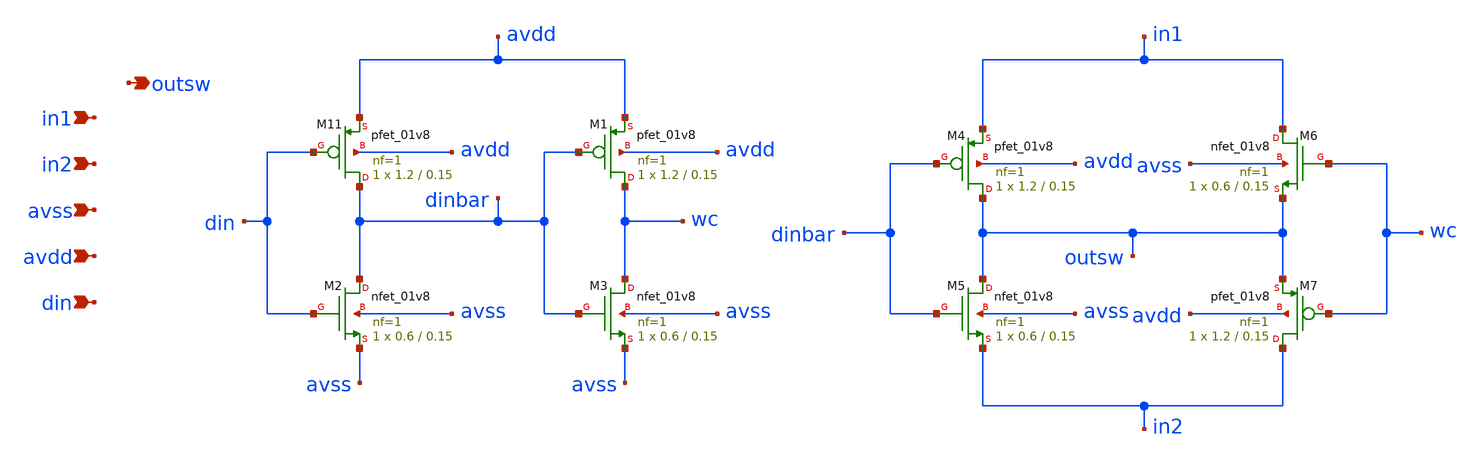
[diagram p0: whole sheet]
** sch_path: xschem/switch.sch
**.subckt switch avss avdd din in1 in2 outsw
*.ipin avss
*.ipin avdd
*.ipin din
*.ipin in1
*.ipin in2
*.opin outsw
XM11 dinbar din avdd avdd sky130_fd_pr__pfet_01v8 L=0.15 W=1.2 nf=1 ad='int((nf+1)/2) * W/nf * 0.29'
+ as='int((nf+2)/2) * W/nf * 0.29' pd='2*int((nf+1)/2) * (W/nf + 0.29)' ps='2*int((nf+2)/2) * (W/nf + 0.29)'
+ nrd='0.29 / W' nrs='0.29 / W' sa=0 sb=0 sd=0 mult=1 m=1
XM1 wc dinbar avdd avdd sky130_fd_pr__pfet_01v8 L=0.15 W=1.2 nf=1 ad='int((nf+1)/2) * W/nf * 0.29' as='int((nf+2)/2) * W/nf * 0.29'
+ pd='2*int((nf+1)/2) * (W/nf + 0.29)' ps='2*int((nf+2)/2) * (W/nf + 0.29)' nrd='0.29 / W' nrs='0.29 / W'
+ sa=0 sb=0 sd=0 mult=1 m=1
XM2 dinbar din avss avss sky130_fd_pr__nfet_01v8 L=0.15 W=0.6 nf=1 ad='int((1 + 1)/2) * 0.6 / 1 * 0.29'
+ as='int((1 + 2)/2) * 0.6 / 1 * 0.29' pd='2*int((1 + 1)/2) * (0.6 / 1 + 0.29)' ps='2*int((1 + 2)/2) * (0.6 / 1 + 0.29)'
+ nrd='0.29 / 0.6 ' nrs='0.29 / 0.6 ' sa=0 sb=0 sd=0 mult=1 m=1
XM3 wc dinbar avss avss sky130_fd_pr__nfet_01v8 L=0.15 W=0.6 nf=1 ad='int((1 + 1)/2) * 0.6 / 1 * 0.29'
+ as='int((1 + 2)/2) * 0.6 / 1 * 0.29' pd='2*int((1 + 1)/2) * (0.6 / 1 + 0.29)' ps='2*int((1 + 2)/2) * (0.6 / 1 + 0.29)'
+ nrd='0.29 / 0.6 ' nrs='0.29 / 0.6 ' sa=0 sb=0 sd=0 mult=1 m=1
XM4 outsw dinbar in1 avdd sky130_fd_pr__pfet_01v8 L=0.15 W=1.2 nf=1 ad='int((nf+1)/2) * W/nf * 0.29'
+ as='int((nf+2)/2) * W/nf * 0.29' pd='2*int((nf+1)/2) * (W/nf + 0.29)' ps='2*int((nf+2)/2) * (W/nf + 0.29)'
+ nrd='0.29 / W' nrs='0.29 / W' sa=0 sb=0 sd=0 mult=1 m=1
XM5 outsw dinbar in2 avss sky130_fd_pr__nfet_01v8 L=0.15 W=0.6 nf=1 ad='int((1 + 1)/2) * 0.6 / 1 * 0.29'
+ as='int((1 + 2)/2) * 0.6 / 1 * 0.29' pd='2*int((1 + 1)/2) * (0.6 / 1 + 0.29)' ps='2*int((1 + 2)/2) * (0.6 / 1 + 0.29)'
+ nrd='0.29 / 0.6 ' nrs='0.29 / 0.6 ' sa=0 sb=0 sd=0 mult=1 m=1
XM6 in1 wc outsw avss sky130_fd_pr__nfet_01v8 L=0.15 W=0.6 nf=1 ad='int((1 + 1)/2) * 0.6 / 1 * 0.29'
+ as='int((1 + 2)/2) * 0.6 / 1 * 0.29' pd='2*int((1 + 1)/2) * (0.6 / 1 + 0.29)' ps='2*int((1 + 2)/2) * (0.6 / 1 + 0.29)'
+ nrd='0.29 / 0.6 ' nrs='0.29 / 0.6 ' sa=0 sb=0 sd=0 mult=1 m=1
XM7 in2 wc outsw avdd sky130_fd_pr__pfet_01v8 L=0.15 W=1.2 nf=1 ad='int((nf+1)/2) * W/nf * 0.29' as='int((nf+2)/2) * W/nf * 0.29'
+ pd='2*int((nf+1)/2) * (W/nf + 0.29)' ps='2*int((nf+2)/2) * (W/nf + 0.29)' nrd='0.29 / W' nrs='0.29 / W'
+ sa=0 sb=0 sd=0 mult=1 m=1
**.ends
.end
